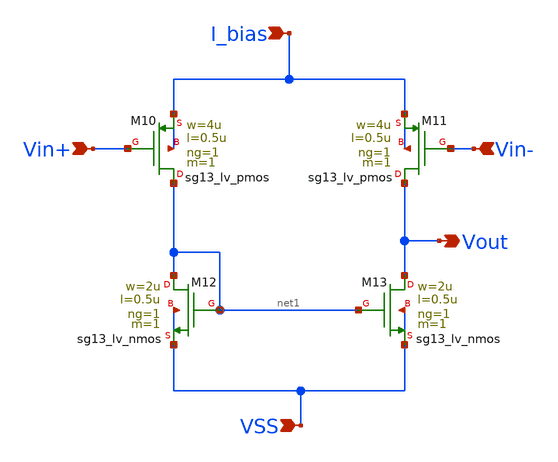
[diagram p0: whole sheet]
** sch_path: SSDOR_1.2V_v2/components/pmos_comp/pmos_comp_2.sch
**.subckt pmos_comp_2 I_bias Vin- Vin+ VSS Vout
*.ipin I_bias
*.ipin Vin-
*.ipin Vin+
*.ipin VSS
*.opin Vout
XM10 net1 Vin+ I_bias I_bias sg13_lv_pmos w=4u l=0.5u ng=1 m=1 mm_ok=1
XM11 Vout Vin- I_bias I_bias sg13_lv_pmos w=4u l=0.5u ng=1 m=1 mm_ok=1
XM12 net1 net1 VSS VSS sg13_lv_nmos w=2u l=0.5u ng=1 m=1 mm_ok=1
XM13 Vout net1 VSS VSS sg13_lv_nmos w=2u l=0.5u ng=1 m=1 mm_ok=1
**.ends
.end
